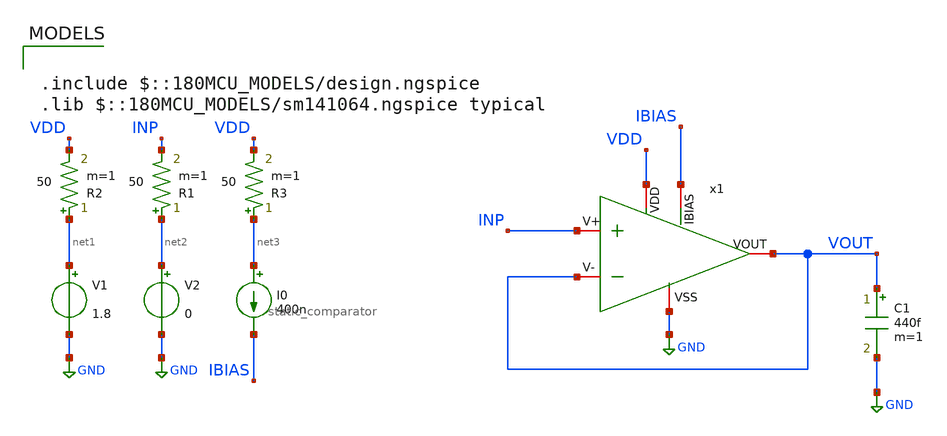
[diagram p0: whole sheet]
** sch_path: designs/static_comparator/xschem/static_comparator_tb_offset.sch
**.subckt static_comparator_tb_offset
V1 net1 GND 1.8
V2 net2 GND 0
C1 VOUT GND 440f m=1
I0 net3 IBIAS 400n
x1 VDD IBIAS GND INP VOUT VOUT static_comparator
R3 net3 VDD 50 m=1
R1 net2 INP 50 m=1
R2 net1 VDD 50 m=1
**** begin user architecture code

.include $::180MCU_MODELS/design.ngspice
.lib $::180MCU_MODELS/sm141064.ngspice typical




.control
save all

**Simulations
op
dc v2 0 1.8 0.01

**Plots
setplot dc1
let VIN = V(INP)
let VOUT = V(VOUT)
plot VOUT

meas dc vout_at_v2_0 find v(VOUT) when v2 = 0

setplot op1
write static_comparator_tb_offset.raw
.endc


**** end user architecture code
**.ends

* expanding   symbol:  gf180/static_comparator/xschem/static_comparator.sym # of pins=6
** sym_path: gf180/static_comparator/xschem/static_comparator.sym
** sch_path: gf180/static_comparator/xschem/static_comparator.sch
.subckt static_comparator VDD IBIAS VSS V+ V- VOUT
*.iopin IBIAS
*.iopin VSS
*.iopin VDD
*.iopin V+
*.iopin V-
*.iopin VOUT
XM1 IBIAS IBIAS VSS VSS nfet_03v3 L=4u W=1.1u nf=1 ad='int((nf+1)/2) * W/nf * 0.18u' as='int((nf+2)/2) * W/nf * 0.18u'
+ pd='2*int((nf+1)/2) * (W/nf + 0.18u)' ps='2*int((nf+2)/2) * (W/nf + 0.18u)' nrd='0.18u / W' nrs='0.18u / W'
+ sa=0 sb=0 sd=0 m=1
XM3 net1 net1 VDD VDD pfet_03v3 L=2u W=4.5u nf=1 ad='int((nf+1)/2) * W/nf * 0.18u' as='int((nf+2)/2) * W/nf * 0.18u'
+ pd='2*int((nf+1)/2) * (W/nf + 0.18u)' ps='2*int((nf+2)/2) * (W/nf + 0.18u)' nrd='0.18u / W' nrs='0.18u / W'
+ sa=0 sb=0 sd=0 m=1
XM2 net1 IBIAS VSS VSS nfet_03v3 L=4u W=625n nf=1 ad='int((nf+1)/2) * W/nf * 0.18u' as='int((nf+2)/2) * W/nf * 0.18u'
+ pd='2*int((nf+1)/2) * (W/nf + 0.18u)' ps='2*int((nf+2)/2) * (W/nf + 0.18u)' nrd='0.18u / W' nrs='0.18u / W'
+ sa=0 sb=0 sd=0 m=1
XM4 net2 net1 VDD VDD pfet_03v3 L=2u W=25u nf=1 ad='int((nf+1)/2) * W/nf * 0.18u' as='int((nf+2)/2) * W/nf * 0.18u'
+ pd='2*int((nf+1)/2) * (W/nf + 0.18u)' ps='2*int((nf+2)/2) * (W/nf + 0.18u)' nrd='0.18u / W' nrs='0.18u / W'
+ sa=0 sb=0 sd=0 m=1
XM5 Vx+ V+ net2 VDD pfet_03v3 L=360n W=2u nf=1 ad='int((nf+1)/2) * W/nf * 0.18u' as='int((nf+2)/2) * W/nf * 0.18u'
+ pd='2*int((nf+1)/2) * (W/nf + 0.18u)' ps='2*int((nf+2)/2) * (W/nf + 0.18u)' nrd='0.18u / W' nrs='0.18u / W'
+ sa=0 sb=0 sd=0 m=10
XM7 Vx+ Vx+ VSS VSS nfet_03v3 L=2u W=985n nf=1 ad='int((nf+1)/2) * W/nf * 0.18u' as='int((nf+2)/2) * W/nf * 0.18u'
+ pd='2*int((nf+1)/2) * (W/nf + 0.18u)' ps='2*int((nf+2)/2) * (W/nf + 0.18u)' nrd='0.18u / W' nrs='0.18u / W'
+ sa=0 sb=0 sd=0 m=1
XM6 Vx- V- net2 VDD pfet_03v3 L=360n W=2u nf=1 ad='int((nf+1)/2) * W/nf * 0.18u' as='int((nf+2)/2) * W/nf * 0.18u'
+ pd='2*int((nf+1)/2) * (W/nf + 0.18u)' ps='2*int((nf+2)/2) * (W/nf + 0.18u)' nrd='0.18u / W' nrs='0.18u / W'
+ sa=0 sb=0 sd=0 m=10
XM8 Vx- Vx- VSS VSS nfet_03v3 L=2u W=985n nf=1 ad='int((nf+1)/2) * W/nf * 0.18u' as='int((nf+2)/2) * W/nf * 0.18u'
+ pd='2*int((nf+1)/2) * (W/nf + 0.18u)' ps='2*int((nf+2)/2) * (W/nf + 0.18u)' nrd='0.18u / W' nrs='0.18u / W'
+ sa=0 sb=0 sd=0 m=1
XM9 net3 net3 VDD VDD pfet_03v3 L=4u W=950n nf=1 ad='int((nf+1)/2) * W/nf * 0.18u' as='int((nf+2)/2) * W/nf * 0.18u'
+ pd='2*int((nf+1)/2) * (W/nf + 0.18u)' ps='2*int((nf+2)/2) * (W/nf + 0.18u)' nrd='0.18u / W' nrs='0.18u / W'
+ sa=0 sb=0 sd=0 m=1
XM10 VOUT net3 VDD VDD pfet_03v3 L=4u W=950n nf=1 ad='int((nf+1)/2) * W/nf * 0.18u' as='int((nf+2)/2) * W/nf * 0.18u'
+ pd='2*int((nf+1)/2) * (W/nf + 0.18u)' ps='2*int((nf+2)/2) * (W/nf + 0.18u)' nrd='0.18u / W' nrs='0.18u / W'
+ sa=0 sb=0 sd=0 m=1
XM11 net3 Vx- VSS VSS nfet_03v3 L=2u W=1.1u nf=1 ad='int((nf+1)/2) * W/nf * 0.18u' as='int((nf+2)/2) * W/nf * 0.18u'
+ pd='2*int((nf+1)/2) * (W/nf + 0.18u)' ps='2*int((nf+2)/2) * (W/nf + 0.18u)' nrd='0.18u / W' nrs='0.18u / W'
+ sa=0 sb=0 sd=0 m=1
XM12 VOUT Vx+ VSS VSS nfet_03v3 L=2u W=1.1u nf=1 ad='int((nf+1)/2) * W/nf * 0.18u' as='int((nf+2)/2) * W/nf * 0.18u'
+ pd='2*int((nf+1)/2) * (W/nf + 0.18u)' ps='2*int((nf+2)/2) * (W/nf + 0.18u)' nrd='0.18u / W' nrs='0.18u / W'
+ sa=0 sb=0 sd=0 m=1
.ends

.GLOBAL GND
.end
